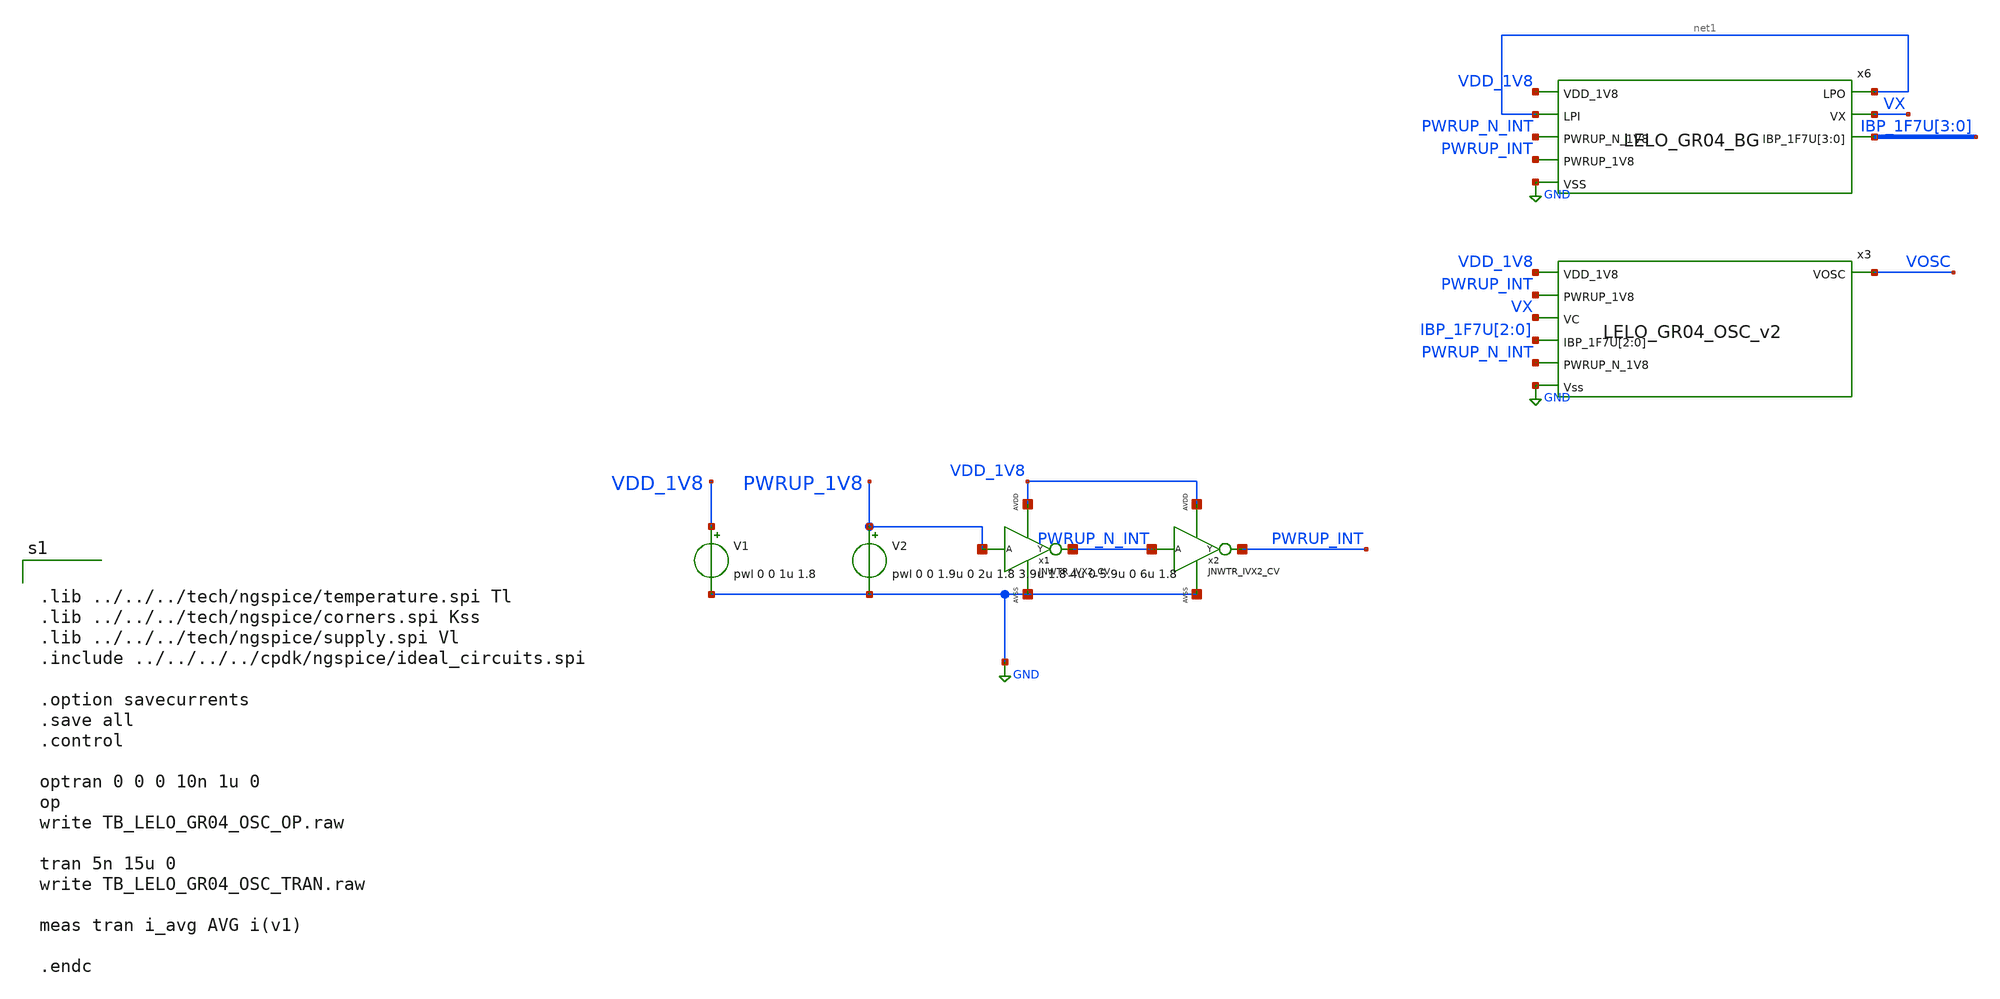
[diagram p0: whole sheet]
** sch_path: design/LELO_GR04_SKY130A/TB_LELO_GR04_OSC.sch
**.subckt TB_LELO_GR04_OSC
V1 VDD_1V8 GND pwl 0 0 1u 1.8
V2 PWRUP_1V8 GND pwl 0 0 1.9u 0 2u 1.8 3.9u 1.8 4u 0 5.9u 0 6u 1.8
x1 PWRUP_1V8 PWRUP_N_INT VDD_1V8 GND JNWTR_IVX2_CV xoffset=0 yoffset=0 angle=0 M=1
x2 PWRUP_N_INT PWRUP_INT VDD_1V8 GND JNWTR_IVX2_CV xoffset=0 yoffset=0 angle=0 M=1
x6 VDD_1V8 net1 net1 VX PWRUP_N_INT IBP_1F7U[3] IBP_1F7U[2] IBP_1F7U[1] IBP_1F7U[0] PWRUP_INT GND
+ LELO_GR04_BG
x3 VDD_1V8 PWRUP_INT VX IBP_1F7U[2] IBP_1F7U[1] IBP_1F7U[0] PWRUP_N_INT GND VOSC LELO_GR04_OSC_v2
**** begin user architecture code


.lib ../../../tech/ngspice/temperature.spi Tl
.lib ../../../tech/ngspice/corners.spi Kss
.lib ../../../tech/ngspice/supply.spi Vl
.include ../../../../cpdk/ngspice/ideal_circuits.spi

.option savecurrents
.save all
.control

optran 0 0 0 10n 1u 0
op
write TB_LELO_GR04_OSC_OP.raw

tran 5n 15u 0
write TB_LELO_GR04_OSC_TRAN.raw

meas tran i_avg AVG i(v1)

.endc


**** end user architecture code
**.ends
.GLOBAL GND
.end
